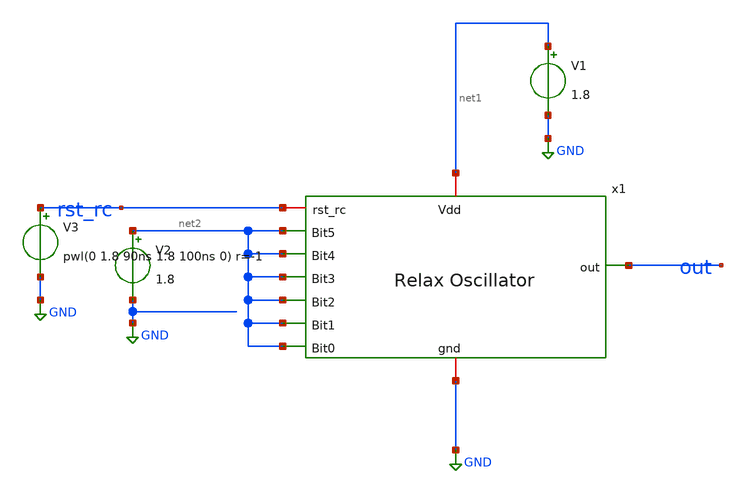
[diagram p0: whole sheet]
** sch_path: xschem/TOP_LEVEL.sch
**.subckt TOP_LEVEL
V1 net1 GND 1.8
V2 net2 GND 1.8
V3 rst_rc GND pwl(0 1.8 90ns 1.8 100ns 0) r=-1
x2 net1 out rst_rc net2 net2 net2 net2 net2 net2 GND relax_oscillator_tb
**** begin user architecture code


.lib /usr/local/share/pdk/sky130A/libs.tech/ngspice/sky130.lib.spice tt
.include /home/lbraga/Projects/relax_oscillator_v2/xschem/relax_oscillator.spice

.control
        tran 0.1n 10000ns
	plot v(rst_rc)
	plot v(out)
	linearize v(out)
	fft v(out)
	plot mag(v(out))
        meas tran iave INTEG i(net1) from=4ns to=5ns
        let power = -iave * 1.8 / 1ns
        print power
.endc
.save all


**** end user architecture code
**.ends
.GLOBAL GND
.end
